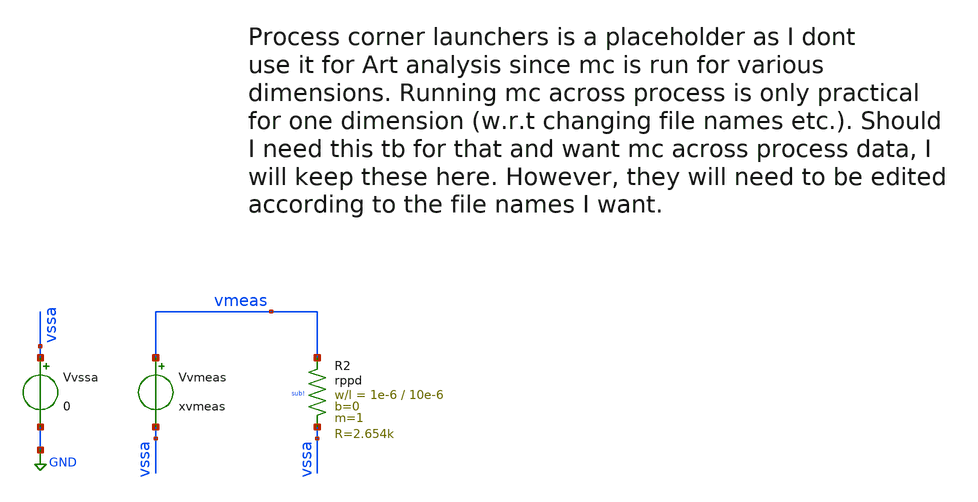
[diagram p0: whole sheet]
** sch_path: tb_res_ihp/tb_res_mc_ihp.sch
**.subckt tb_res_mc_ihp
Vvssa vssa GND 0
Vvmeas vmeas vssa xvmeas
XR2 vmeas vssa sub! rppd w=1e-6 l=10e-6 m=1 b=0 mm_ok=1
**** begin user architecture code

** opencircuitdesign pdks install
.lib /home/slice/pdk/iHP/IHP-Open-PDK/ihp-sg13g2/libs.tech/ngspice/models/cornerRES.lib res_typ_mismatch

* Parameters

.param xvmeas = 1
.csparam xvmeas_var = 'xvmeas'
.param xtsim = 5u
.csparam xtsim_var = 'xtsim'
.temp 27

  .save v(vmeas) i(Vvmeas)

  .control

    let run = 1

    dowhile run <= 100
    reset

** 1. TRAN ANALYSIS **

  tran 1n $&xtsim_var

** 2. MEASURES **

  meas tran vmeas_avg AVG vmeas
  meas tran imeas_avg AVG i(Vvmeas)
  let rmeas = (vmeas_avg/imeas_avg)*-1
  echo "$&rmeas"
  echo "$&rmeas" >> res_measures_typ_mc.txt

    remzerovec
    set filetype=binary
    ** first write deletes existing file
    write tb_res_ihp_mc.raw
    ** set appendwrite appends following writes to existing raw file
    set appendwrite
    let run = run+1

    end

  setplot
quit 0
.endc




**** end user architecture code
**.ends
.GLOBAL GND
.end
